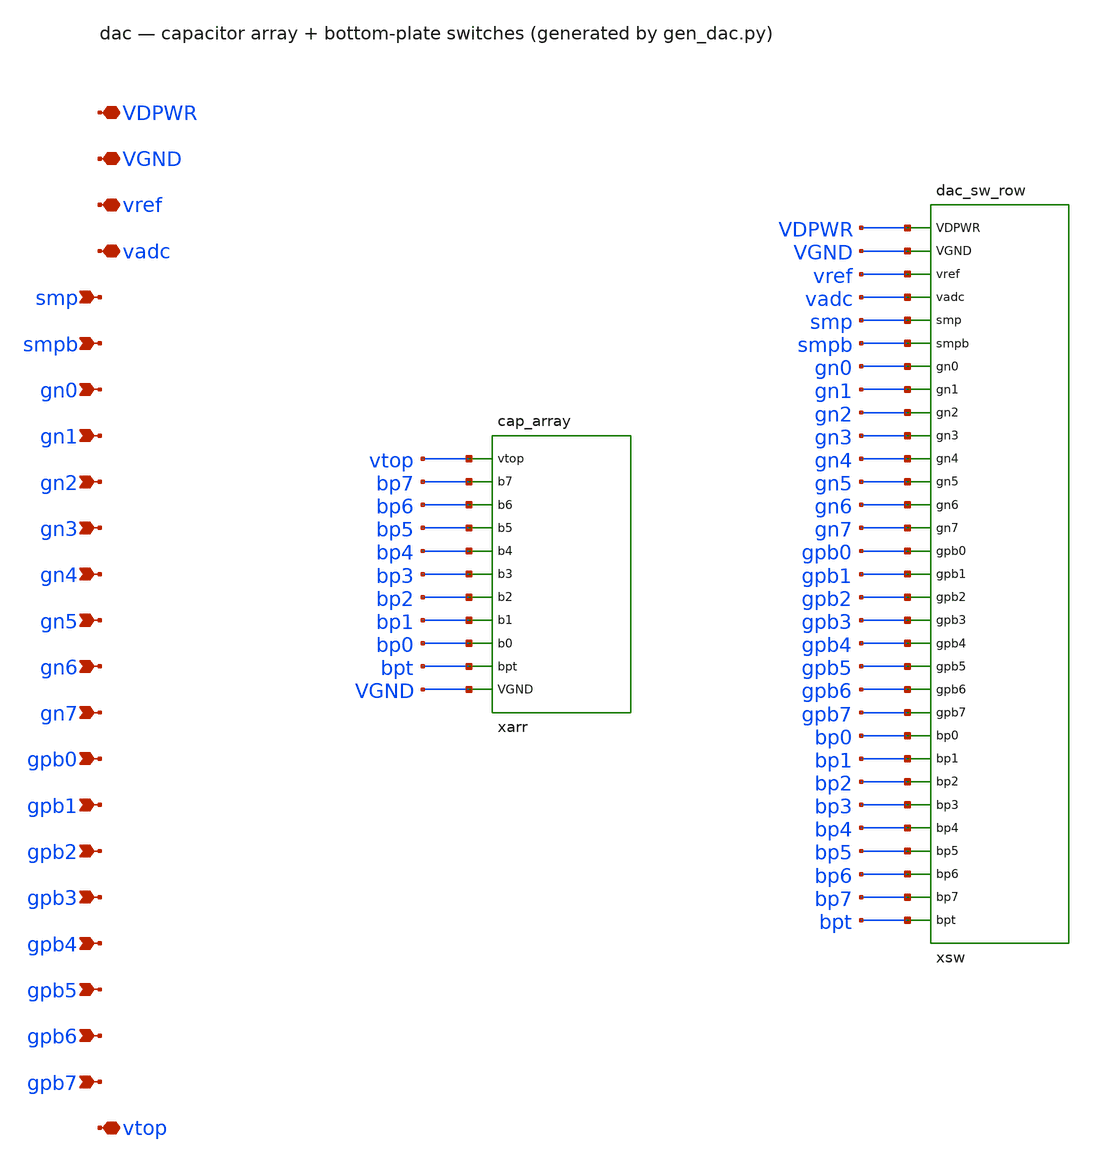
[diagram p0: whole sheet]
** sch_path: xschem/dac.sch
**.subckt dac VDPWR VGND vref vadc smp smpb gn0 gn1 gn2 gn3 gn4 gn5 gn6 gn7 gpb0 gpb1 gpb2 gpb3 gpb4
*+ gpb5 gpb6 gpb7 vtop
*.iopin VDPWR
*.iopin VGND
*.iopin vref
*.iopin vadc
*.ipin smp
*.ipin smpb
*.ipin gn0
*.ipin gn1
*.ipin gn2
*.ipin gn3
*.ipin gn4
*.ipin gn5
*.ipin gn6
*.ipin gn7
*.ipin gpb0
*.ipin gpb1
*.ipin gpb2
*.ipin gpb3
*.ipin gpb4
*.ipin gpb5
*.ipin gpb6
*.ipin gpb7
*.iopin vtop
xarr vtop bp7 bp6 bp5 bp4 bp3 bp2 bp1 bp0 bpt VGND cap_array
xsw VDPWR VGND vref vadc smp smpb gn0 gn1 gn2 gn3 gn4 gn5 gn6 gn7 gpb0 gpb1 gpb2 gpb3 gpb4 gpb5 gpb6
+ gpb7 bp0 bp1 bp2 bp3 bp4 bp5 bp6 bp7 bpt dac_sw_row
**.ends

* expanding   symbol:  cap_array.sym # of pins=11
** sym_path: xschem/cap_array.sym
** sch_path: xschem/cap_array.sch
.subckt cap_array vtop b7 b6 b5 b4 b3 b2 b1 b0 bpt VGND
*.iopin vtop
*.iopin b7
*.iopin b6
*.iopin b5
*.iopin b4
*.iopin b3
*.iopin b2
*.iopin b1
*.iopin b0
*.iopin bpt
*.iopin VGND
XC7 vtop b7 sky130_fd_pr__cap_mim_m3_1 W=2 L=1.65 MF=128 m=128
XC6 vtop b6 sky130_fd_pr__cap_mim_m3_1 W=2 L=1.65 MF=64 m=64
XC5 vtop b5 sky130_fd_pr__cap_mim_m3_1 W=2 L=1.65 MF=32 m=32
XC4 vtop b4 sky130_fd_pr__cap_mim_m3_1 W=2 L=1.65 MF=16 m=16
XC3 vtop b3 sky130_fd_pr__cap_mim_m3_1 W=2 L=1.65 MF=8 m=8
XC2 vtop b2 sky130_fd_pr__cap_mim_m3_1 W=2 L=1.65 MF=4 m=4
XC1 vtop b1 sky130_fd_pr__cap_mim_m3_1 W=2 L=1.65 MF=2 m=2
XC0 vtop b0 sky130_fd_pr__cap_mim_m3_1 W=2 L=1.65 MF=1 m=1
XCT vtop bpt sky130_fd_pr__cap_mim_m3_1 W=2 L=1.65 MF=1 m=1
XCD VGND VGND sky130_fd_pr__cap_mim_m3_1 W=2 L=1.65 MF=32 m=32
.ends


* expanding   symbol:  dac_sw_row.sym # of pins=31
** sym_path: xschem/dac_sw_row.sym
** sch_path: xschem/dac_sw_row.sch
.subckt dac_sw_row VDPWR VGND vref vadc smp smpb gn0 gn1 gn2 gn3 gn4 gn5 gn6 gn7 gpb0 gpb1 gpb2 gpb3
+ gpb4 gpb5 gpb6 gpb7 bp0 bp1 bp2 bp3 bp4 bp5 bp6 bp7 bpt
*.iopin VDPWR
*.iopin VGND
*.iopin vref
*.iopin vadc
*.ipin smp
*.ipin smpb
*.ipin gn0
*.ipin gn1
*.ipin gn2
*.ipin gn3
*.ipin gn4
*.ipin gn5
*.ipin gn6
*.ipin gn7
*.ipin gpb0
*.ipin gpb1
*.ipin gpb2
*.ipin gpb3
*.ipin gpb4
*.ipin gpb5
*.ipin gpb6
*.ipin gpb7
*.iopin bp0
*.iopin bp1
*.iopin bp2
*.iopin bp3
*.iopin bp4
*.iopin bp5
*.iopin bp6
*.iopin bp7
*.iopin bpt
xsw_bp7 VDPWR VGND vref vadc smp smpb gn7 gpb7 bp7 dac_sw
xsw_bp6 VDPWR VGND vref vadc smp smpb gn6 gpb6 bp6 dac_sw
xsw_bp5 VDPWR VGND vref vadc smp smpb gn5 gpb5 bp5 dac_sw
xsw_bp4 VDPWR VGND vref vadc smp smpb gn4 gpb4 bp4 dac_sw
xsw_bp3 VDPWR VGND vref vadc smp smpb gn3 gpb3 bp3 dac_sw
xsw_bp2 VDPWR VGND vref vadc smp smpb gn2 gpb2 bp2 dac_sw
xsw_bp1 VDPWR VGND vref vadc smp smpb gn1 gpb1 bp1 dac_sw
xsw_bp0 VDPWR VGND vref vadc smp smpb gn0 gpb0 bp0 dac_sw
xsw_bpt VDPWR VGND vref vadc smp smpb smpb VDPWR bpt dac_sw
.ends


* expanding   symbol:  dac_sw.sym # of pins=9
** sym_path: xschem/dac_sw.sym
** sch_path: xschem/dac_sw.sch
.subckt dac_sw VDPWR VGND vref vadc smp smpb gn gpb bp
*.iopin VDPWR
*.iopin VGND
*.iopin vref
*.iopin vadc
*.ipin smp
*.ipin smpb
*.ipin gn
*.ipin gpb
*.iopin bp
XMSG bp gn VGND VGND sky130_fd_pr__nfet_01v8 L=0.15 W=1 nf=1 ad='int((1 + 1)/2) * 1 / 1 * 0.29' as='int((1 + 2)/2) * 1 / 1 * 0.29'
+ pd='2*int((1 + 1)/2) * (1 / 1 + 0.29)' ps='2*int((1 + 2)/2) * (1 / 1 + 0.29)' nrd='0.29 / 1 ' nrs='0.29 / 1 '
+ sa=0 sb=0 sd=0 mult=1 m=1
XMSR bp gpb vref VDPWR sky130_fd_pr__pfet_01v8_lvt L=0.35 W=4 nf=1 ad='int((1 + 1)/2) * 4 / 1 * 0.29'
+ as='int((1 + 2)/2) * 4 / 1 * 0.29' pd='2*int((1 + 1)/2) * (4 / 1 + 0.29)' ps='2*int((1 + 2)/2) * (4 / 1 + 0.29)'
+ nrd='0.29 / 4 ' nrs='0.29 / 4 ' sa=0 sb=0 sd=0 mult=1 m=1
XMSN bp smp vadc VGND sky130_fd_pr__nfet_01v8 L=0.15 W=1 nf=1 ad='int((1 + 1)/2) * 1 / 1 * 0.29' as='int((1 + 2)/2) * 1 / 1 * 0.29'
+ pd='2*int((1 + 1)/2) * (1 / 1 + 0.29)' ps='2*int((1 + 2)/2) * (1 / 1 + 0.29)' nrd='0.29 / 1 ' nrs='0.29 / 1 '
+ sa=0 sb=0 sd=0 mult=1 m=1
XMSP bp smpb vadc VDPWR sky130_fd_pr__pfet_01v8_lvt L=0.35 W=2 nf=1 ad='int((1 + 1)/2) * 2 / 1 * 0.29'
+ as='int((1 + 2)/2) * 2 / 1 * 0.29' pd='2*int((1 + 1)/2) * (2 / 1 + 0.29)' ps='2*int((1 + 2)/2) * (2 / 1 + 0.29)'
+ nrd='0.29 / 2 ' nrs='0.29 / 2 ' sa=0 sb=0 sd=0 mult=1 m=1
.ends

.end
